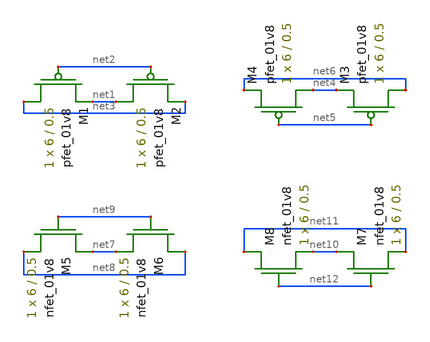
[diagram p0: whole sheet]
** sch_path: mp3/schematic/untitled.sch
**.subckt untitled
XM1 net3 net2 net1 VDD sky130_fd_pr__pfet_01v8 L=0.5 W=6 nf=1 ad='int((nf+1)/2) * W/nf * 0.29' as='int((nf+2)/2) * W/nf * 0.29'
+ pd='2*int((nf+1)/2) * (W/nf + 0.29)' ps='2*int((nf+2)/2) * (W/nf + 0.29)' nrd='0.29 / W' nrs='0.29 / W'
+ sa=0 sb=0 sd=0 mult=1 m=1
XM2 net1 net2 net3 VDD sky130_fd_pr__pfet_01v8 L=0.5 W=6 nf=1 ad='int((nf+1)/2) * W/nf * 0.29' as='int((nf+2)/2) * W/nf * 0.29'
+ pd='2*int((nf+1)/2) * (W/nf + 0.29)' ps='2*int((nf+2)/2) * (W/nf + 0.29)' nrd='0.29 / W' nrs='0.29 / W'
+ sa=0 sb=0 sd=0 mult=1 m=1
XM3 net6 net5 net4 VDD sky130_fd_pr__pfet_01v8 L=0.5 W=6 nf=1 ad='int((nf+1)/2) * W/nf * 0.29' as='int((nf+2)/2) * W/nf * 0.29'
+ pd='2*int((nf+1)/2) * (W/nf + 0.29)' ps='2*int((nf+2)/2) * (W/nf + 0.29)' nrd='0.29 / W' nrs='0.29 / W'
+ sa=0 sb=0 sd=0 mult=1 m=1
XM4 net4 net5 net6 VDD sky130_fd_pr__pfet_01v8 L=0.5 W=6 nf=1 ad='int((nf+1)/2) * W/nf * 0.29' as='int((nf+2)/2) * W/nf * 0.29'
+ pd='2*int((nf+1)/2) * (W/nf + 0.29)' ps='2*int((nf+2)/2) * (W/nf + 0.29)' nrd='0.29 / W' nrs='0.29 / W'
+ sa=0 sb=0 sd=0 mult=1 m=1
XM5 net7 net9 net8 GND sky130_fd_pr__nfet_01v8 L=0.5 W=6 nf=1 ad='int((nf+1)/2) * W/nf * 0.29' as='int((nf+2)/2) * W/nf * 0.29'
+ pd='2*int((nf+1)/2) * (W/nf + 0.29)' ps='2*int((nf+2)/2) * (W/nf + 0.29)' nrd='0.29 / W' nrs='0.29 / W'
+ sa=0 sb=0 sd=0 mult=1 m=1
XM6 net8 net9 net7 GND sky130_fd_pr__nfet_01v8 L=0.5 W=6 nf=1 ad='int((nf+1)/2) * W/nf * 0.29' as='int((nf+2)/2) * W/nf * 0.29'
+ pd='2*int((nf+1)/2) * (W/nf + 0.29)' ps='2*int((nf+2)/2) * (W/nf + 0.29)' nrd='0.29 / W' nrs='0.29 / W'
+ sa=0 sb=0 sd=0 mult=1 m=1
XM7 net10 net12 net11 GND sky130_fd_pr__nfet_01v8 L=0.5 W=6 nf=1 ad='int((nf+1)/2) * W/nf * 0.29' as='int((nf+2)/2) * W/nf * 0.29'
+ pd='2*int((nf+1)/2) * (W/nf + 0.29)' ps='2*int((nf+2)/2) * (W/nf + 0.29)' nrd='0.29 / W' nrs='0.29 / W'
+ sa=0 sb=0 sd=0 mult=1 m=1
XM8 net11 net12 net10 GND sky130_fd_pr__nfet_01v8 L=0.5 W=6 nf=1 ad='int((nf+1)/2) * W/nf * 0.29' as='int((nf+2)/2) * W/nf * 0.29'
+ pd='2*int((nf+1)/2) * (W/nf + 0.29)' ps='2*int((nf+2)/2) * (W/nf + 0.29)' nrd='0.29 / W' nrs='0.29 / W'
+ sa=0 sb=0 sd=0 mult=1 m=1
**.ends
.end
